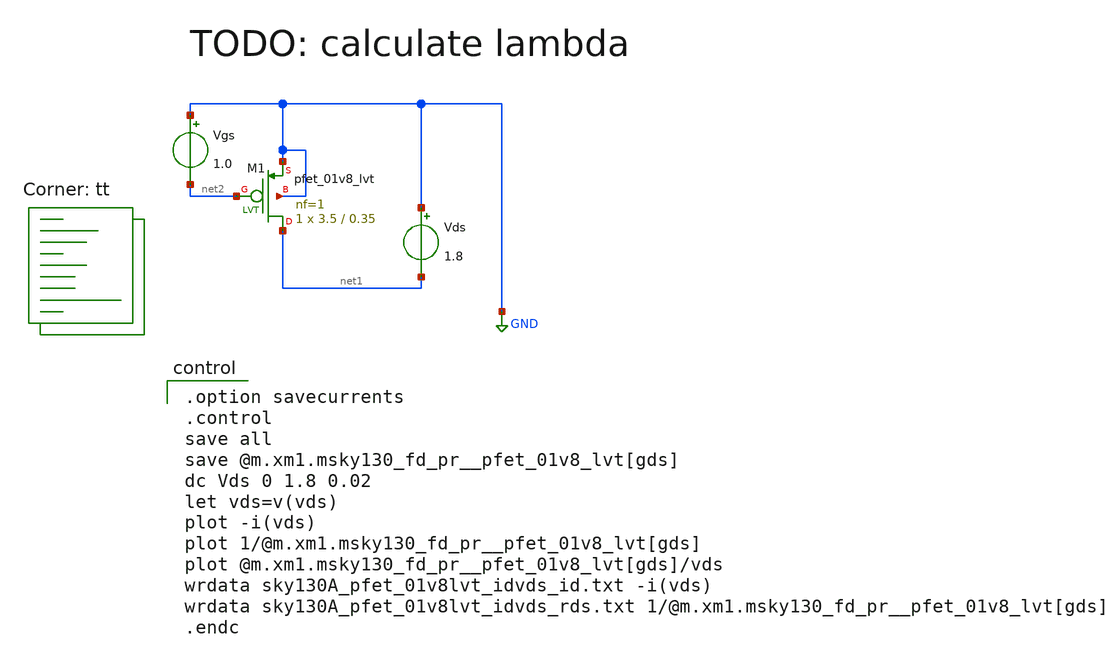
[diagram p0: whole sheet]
** sch_path: xschem/MOSFET/sky130A_pfet_01v8lvt_idvds.sch
**.subckt sky130A_pfet_01v8lvt_idvds
Vgs GND net2 1.0
Vds GND net1 1.8
XM1 net1 net2 GND GND sky130_fd_pr__pfet_01v8_lvt L=0.35 W=3.5 nf=1 ad='int((1 + 1)/2) * 3.5 / 1 * 0.29'
+ as='int((1 + 2)/2) * 3.5 / 1 * 0.29' pd='2*int((1 + 1)/2) * (3.5 / 1 + 0.29)' ps='2*int((1 + 2)/2) * (3.5 / 1 + 0.29)'
+ nrd='0.29 / 3.5 ' nrs='0.29 / 3.5 ' sa=0 sb=0 sd=0 mult=1 m=1
**** begin user architecture code

.option savecurrents
.control
save all
save @m.xm1.msky130_fd_pr__pfet_01v8_lvt[gds]
dc Vds 0 1.8 0.02
let vds=v(vds)
plot -i(vds)
plot 1/@m.xm1.msky130_fd_pr__pfet_01v8_lvt[gds]
plot @m.xm1.msky130_fd_pr__pfet_01v8_lvt[gds]/vds
wrdata sky130A_pfet_01v8lvt_idvds_id.txt -i(vds)
wrdata sky130A_pfet_01v8lvt_idvds_rds.txt 1/@m.xm1.msky130_fd_pr__pfet_01v8_lvt[gds]
.endc

.lib $::SKYWATER_MODELS/sky130.lib.spice tt
**** end user architecture code
**.ends
.GLOBAL GND
.end
